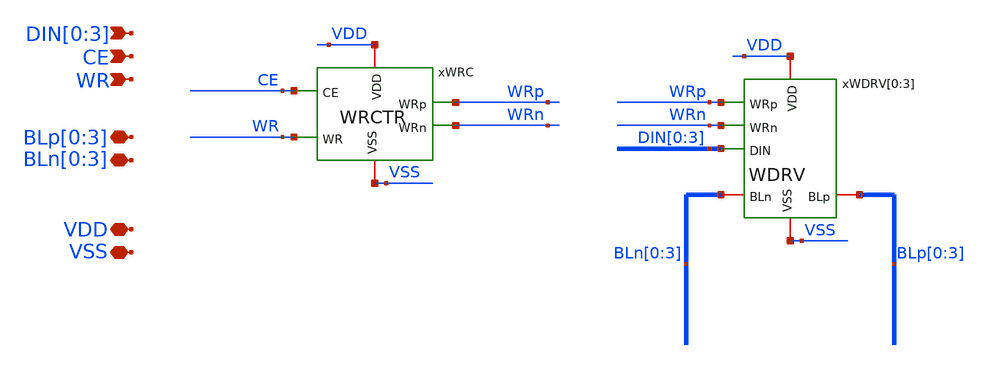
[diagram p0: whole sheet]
** sch_path: module/SRAM128/schematic/SRAM_WD4.sch
**.subckt SRAM_WD4 CE DIN[0],DIN[1],DIN[2],DIN[3] VSS VDD WR BLn[0],BLn[1],BLn[2],BLn[3]
*+ BLp[0],BLp[1],BLp[2],BLp[3]
*.ipin CE
*.ipin DIN[0],DIN[1],DIN[2],DIN[3]
*.iopin VSS
*.iopin VDD
*.ipin WR
*.iopin BLn[0],BLn[1],BLn[2],BLn[3]
*.iopin BLp[0],BLp[1],BLp[2],BLp[3]
xWDRV[0] VDD WRn BLp[0] BLn[0] WRp VSS DIN[0] WDRV
xWDRV[1] VDD WRn BLp[1] BLn[1] WRp VSS DIN[1] WDRV
xWDRV[2] VDD WRn BLp[2] BLn[2] WRp VSS DIN[2] WDRV
xWDRV[3] VDD WRn BLp[3] BLn[3] WRp VSS DIN[3] WDRV
xWRC VDD VSS WRn CE WR WRp WRCTR
**.ends

* expanding   symbol:  WDRV.sym # of pins=7
** sym_path: module/SRAM128/schematic/WDRV.sym
** sch_path: module/SRAM128/schematic/WDRV.sch
.subckt WDRV VDD WRn BLp BLn WRp VSS DIN
*.iopin BLn
*.iopin BLp
*.ipin DIN
*.ipin WRn
*.ipin WRp
*.iopin VDD
*.iopin VSS
XXM1 BLn WRp net2 VSS NMOS w=5.4u l=1u as=0 ad=0 ps=0 pd=0 nrd=0 nrs=0 m=1
XXM2 net2 Dp VSS VSS NMOS w=5.4u l=1u as=0 ad=0 ps=0 pd=0 nrd=0 nrs=0 m=1
XXM3 net1 Dp VDD VDD PMOS w=9.4u l=1u as=0 ad=0 ps=0 pd=0 nrd=0 nrs=0 m=1
XXM4 BLn WRn net1 VDD PMOS w=9.4u l=1u as=0 ad=0 ps=0 pd=0 nrd=0 nrs=0 m=1
XXM5 Dp Dn VDD VDD PMOS w=6.8u l=1u as=0 ad=0 ps=0 pd=0 nrd=0 nrs=0 m=1
XXM6 Dp Dn VSS VSS NMOS w=3.4u l=1u as=0 ad=0 ps=0 pd=0 nrd=0 nrs=0 m=1
XXM7 BLp WRp net4 VSS NMOS w=5.4u l=1u as=0 ad=0 ps=0 pd=0 nrd=0 nrs=0 m=1
XXM8 net4 Dn VSS VSS NMOS w=5.4u l=1u as=0 ad=0 ps=0 pd=0 nrd=0 nrs=0 m=1
XXM9 net3 Dn VDD VDD PMOS w=9.4u l=1u as=0 ad=0 ps=0 pd=0 nrd=0 nrs=0 m=1
XXM10 BLp WRn net3 VDD PMOS w=9.4u l=1u as=0 ad=0 ps=0 pd=0 nrd=0 nrs=0 m=1
XXM11 Dn DIN VDD VDD PMOS w=6.8u l=1u as=0 ad=0 ps=0 pd=0 nrd=0 nrs=0 m=1
XXM12 Dn DIN VSS VSS NMOS w=3.4u l=1u as=0 ad=0 ps=0 pd=0 nrd=0 nrs=0 m=1
.ends


* expanding   symbol:  WRCTR.sym # of pins=6
** sym_path: module/SRAM128/schematic/WRCTR.sym
** sch_path: module/SRAM128/schematic/WRCTR.sch
.subckt WRCTR VDD VSS WRn CE WR WRp
*.opin WRn
*.ipin CE
*.iopin VDD
*.iopin VSS
*.ipin WR
*.opin WRp
XXM1 WRp net1 VSS VSS NMOS w=6.8u l=1u as=0 ad=0 ps=0 pd=0 nrd=0 nrs=0 m=1
XXM4 WRp net1 VDD VDD PMOS w=6.8u l=1u as=0 ad=0 ps=0 pd=0 nrd=0 nrs=0 m=1
XXM2 net1 net2 net3 VSS NMOS w=3.4u l=1u as=0 ad=0 ps=0 pd=0 nrd=0 nrs=0 m=1
XXM17 net1 net2 VDD VDD PMOS w=3.4u l=1u as=0 ad=0 ps=0 pd=0 nrd=0 nrs=0 m=1
XXM18 net3 WR VSS VSS NMOS w=3.4u l=1u as=0 ad=0 ps=0 pd=0 nrd=0 nrs=0 m=1
XXM19 net1 WR VDD VDD PMOS w=3.4u l=1u as=0 ad=0 ps=0 pd=0 nrd=0 nrs=0 m=1
XXM5 WRn WRp VSS VSS NMOS w=6.8u l=1u as=0 ad=0 ps=0 pd=0 nrd=0 nrs=0 m=1
XXM6 WRn WRp VDD VDD PMOS w=6.8u l=1u as=0 ad=0 ps=0 pd=0 nrd=0 nrs=0 m=1
XXM3 net2 net4 VSS VSS NMOS w=3.4u l=1u as=0 ad=0 ps=0 pd=0 nrd=0 nrs=0 m=1
XXM7 net2 net4 VDD VDD PMOS w=3.4u l=1u as=0 ad=0 ps=0 pd=0 nrd=0 nrs=0 m=1
XXM8 net4 CE VSS VSS NMOS w=3.4u l=1u as=0 ad=0 ps=0 pd=0 nrd=0 nrs=0 m=1
XXM9 net4 CE VDD VDD PMOS w=3.4u l=1u as=0 ad=0 ps=0 pd=0 nrd=0 nrs=0 m=1
.ends

.end
